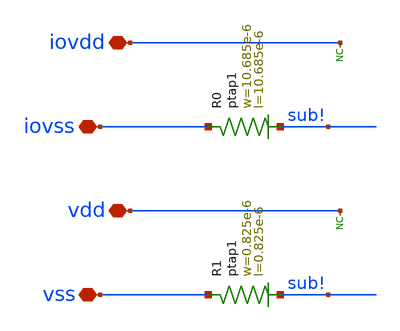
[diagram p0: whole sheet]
** sch_path: ihp-sg13g2/libs.ref/sg13g2_io/sch/xschem/sg13g2_Filler400.sch
**.subckt sg13g2_Filler400 iovdd iovss vdd vss
*.iopin iovdd
*.iopin iovss
*.iopin vdd
*.iopin vss
* noconn iovdd
* noconn vdd
XR0 iovss sub! ptap1 R=6.246 w=10.685e-6 l=10.685e-6
XR1 vss sub! ptap1 R=246.2 w=0.825e-6 l=0.825e-6
**.ends
.end
